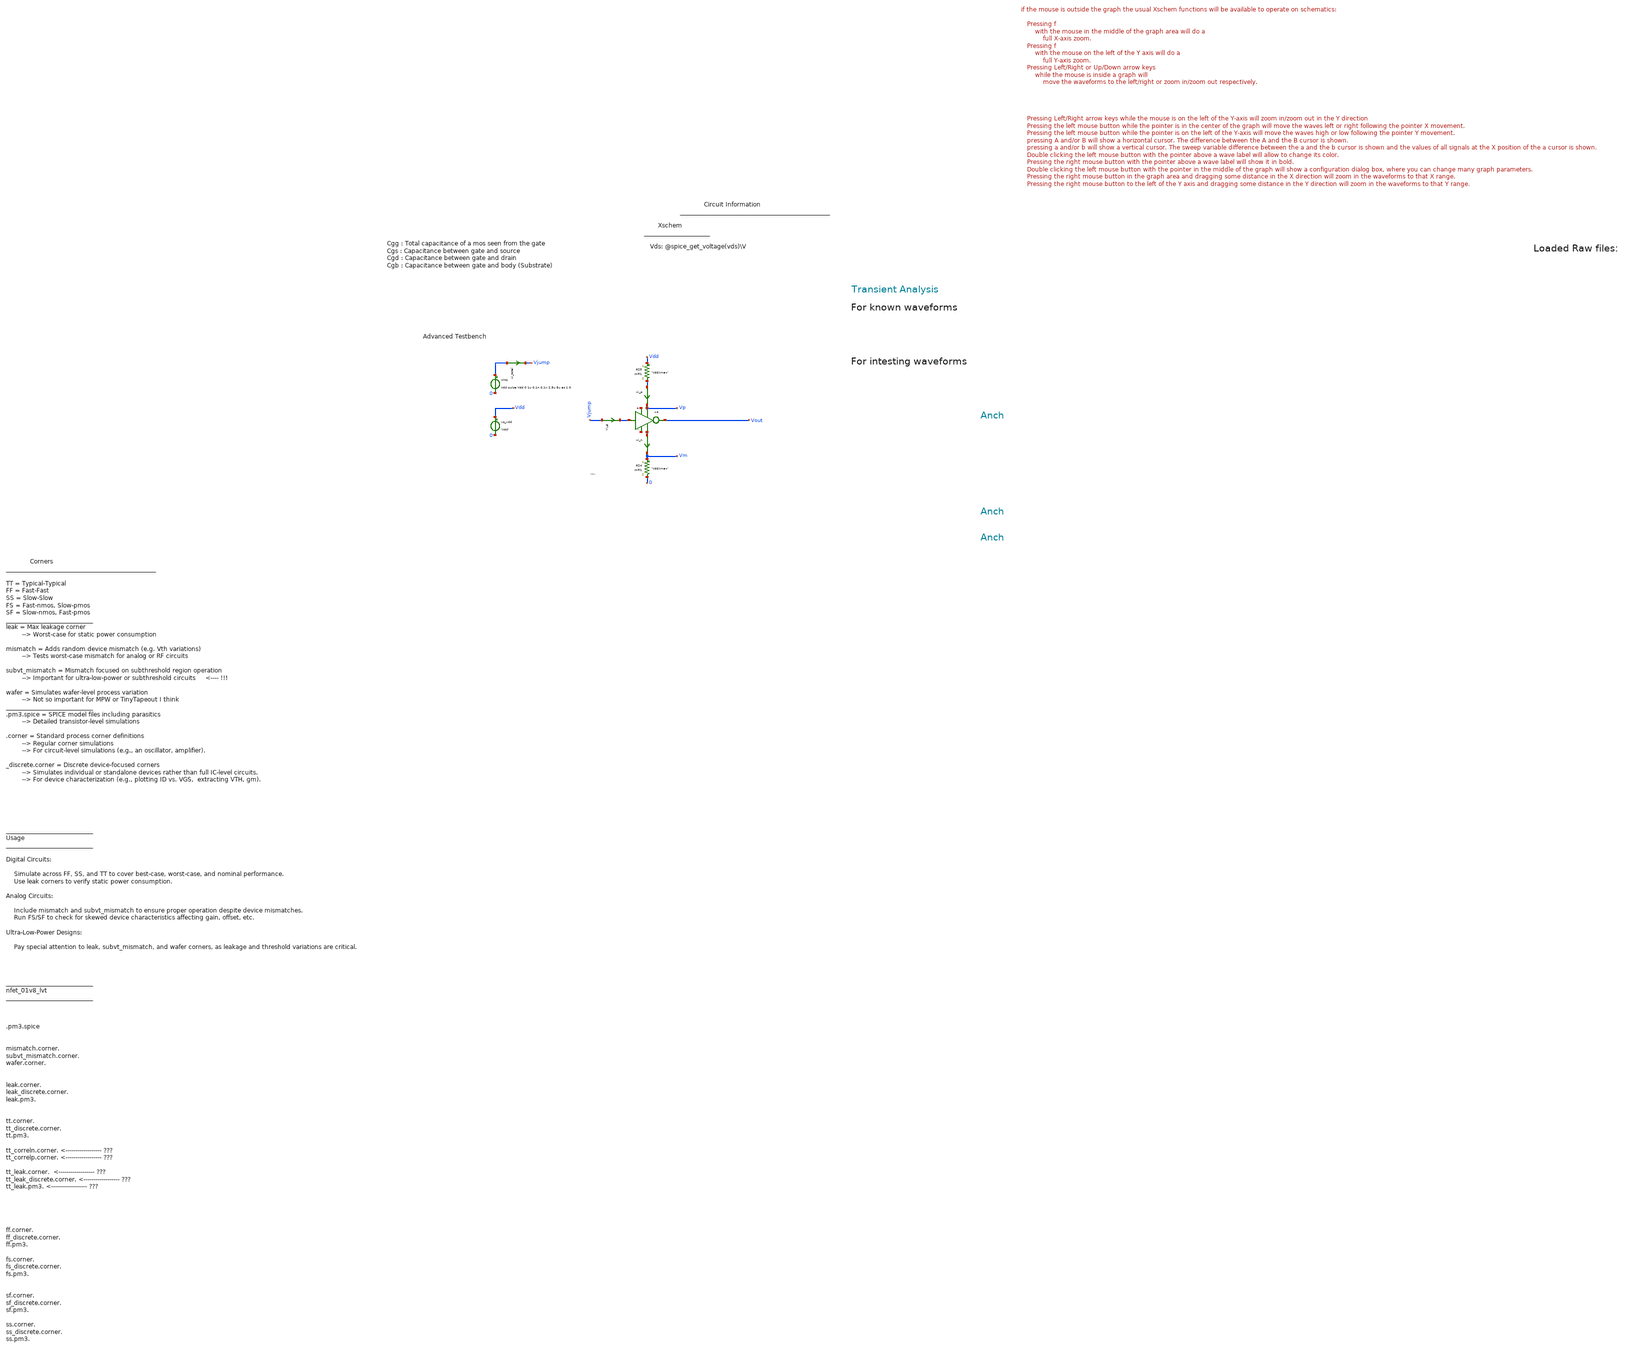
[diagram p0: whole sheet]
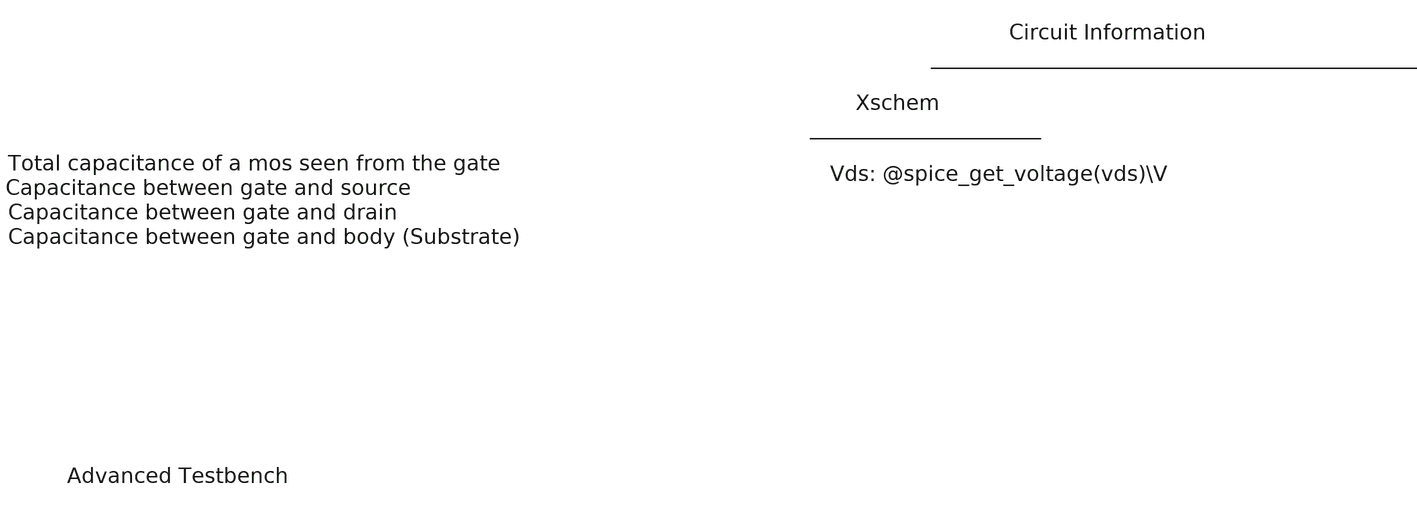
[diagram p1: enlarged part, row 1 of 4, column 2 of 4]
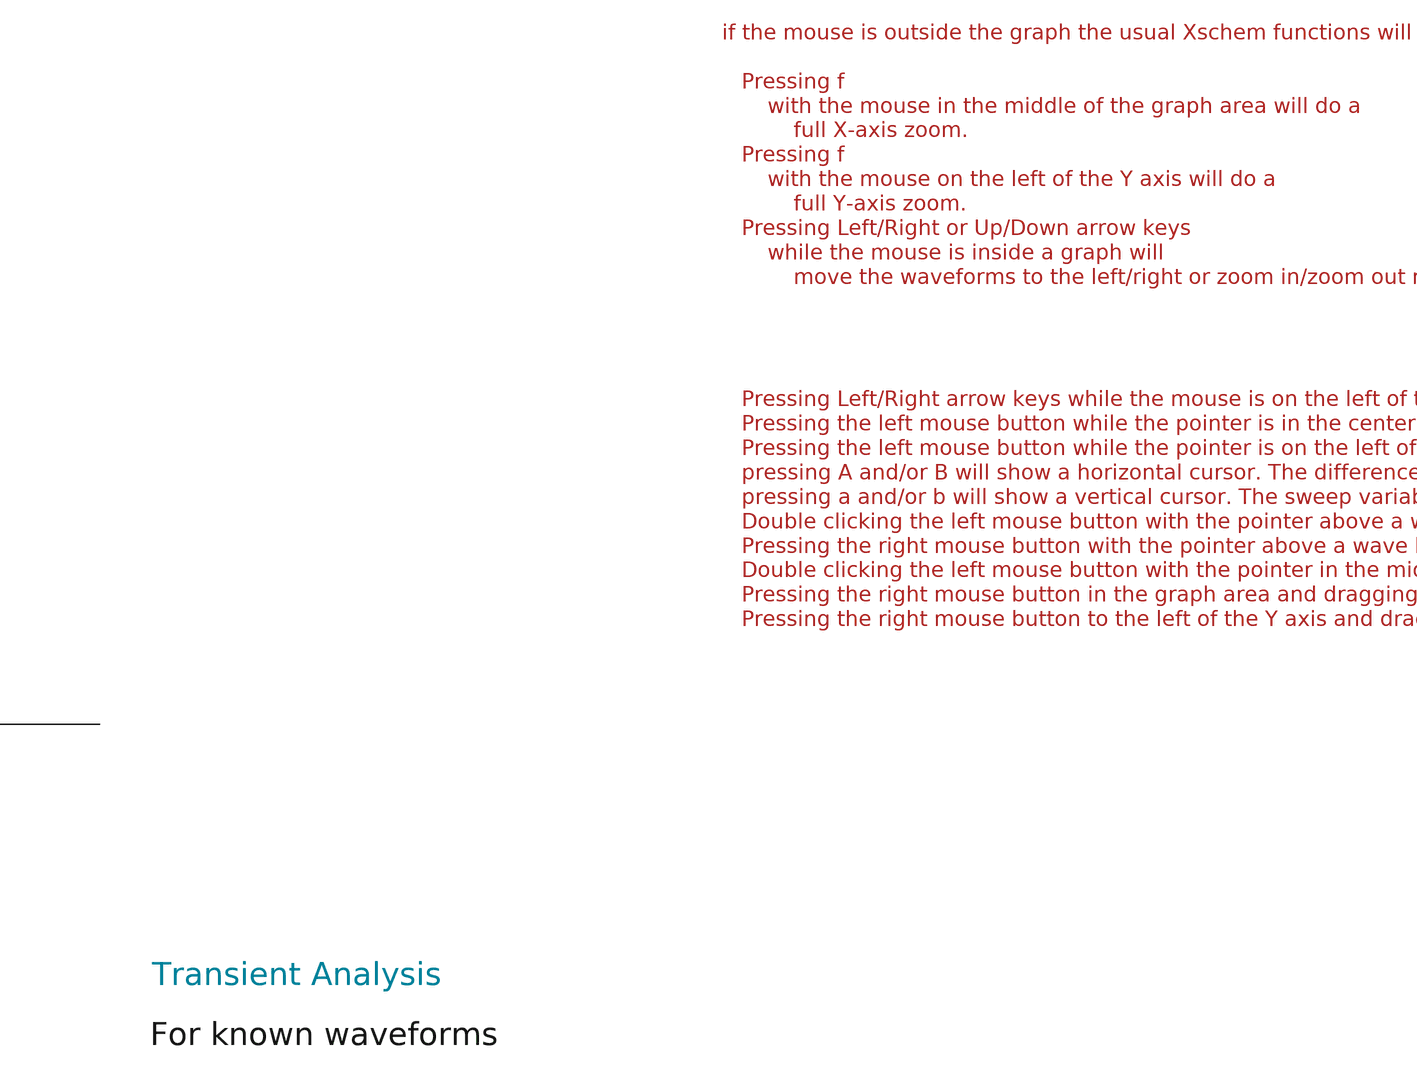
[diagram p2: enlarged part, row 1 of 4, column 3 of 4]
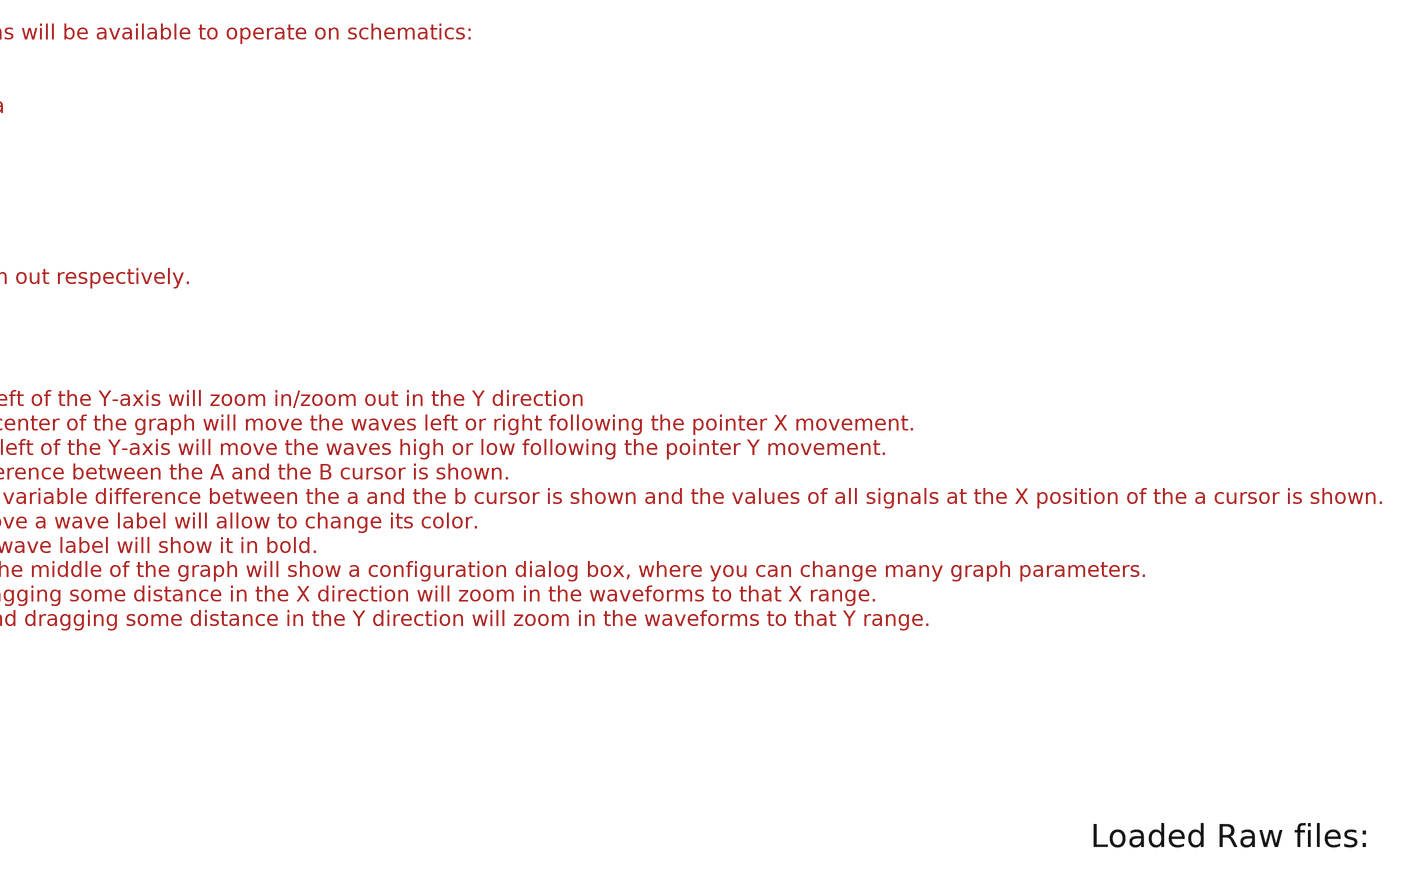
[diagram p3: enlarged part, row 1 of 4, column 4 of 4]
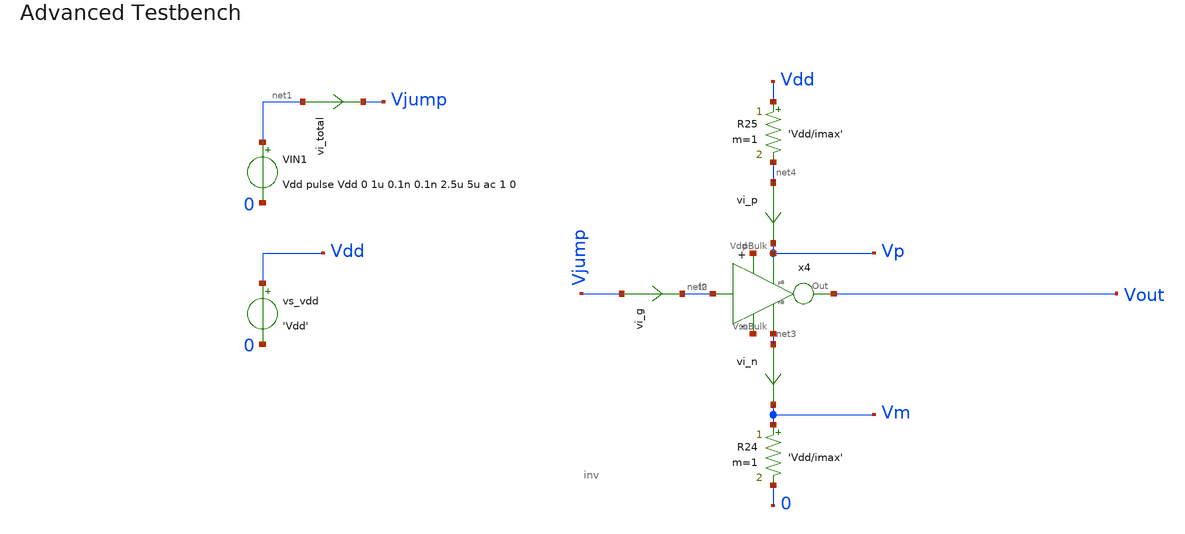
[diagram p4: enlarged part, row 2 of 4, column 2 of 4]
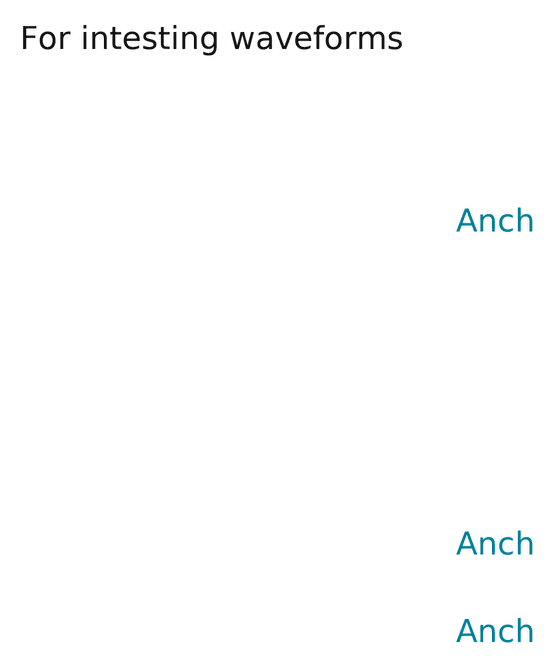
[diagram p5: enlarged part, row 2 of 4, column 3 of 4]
** sch_path: tt10-hdl/tt_um_test_commit/xschem/T0/inv/inv_Slewrate_tb.sch
* Copyright (C) 1998-2024 Stefan Frederik Schippers
* This program is free software; you can redistribute it and/or modify
* it under the terms of the GNU General Public License as published by
* the Free Software Foundation; either version 2 of the License, or
* (at your option) any later version.
* This program is distributed in the hope that it will be useful,
* but WITHOUT ANY WARRANTY; without even the implied warranty of
* MERCHANTABILITY or FITNESS FOR A PARTICULAR PURPOSE.  See the
* GNU General Public License for more details.
* You should have received a copy of the GNU General Public License
* along with this program; if not, write to the Free Software
**.subckt inv_Slewrate_tb
VIN1 net1 0 Vdd pulse Vdd 0 1u 0.1n 0.1n 2.5u 5u ac 1 0
vi_total net1 Vjump 0
.save i(vi_total)
vs_vdd Vdd 0 'Vdd'
x4 net5 net6 Vout net2 net3 Vp inv
vi_g Vjump net2 0
.save i(vi_g)
vi_p net4 Vp 0
.save i(vi_p)
vi_n net3 Vm 0
.save i(vi_n)
R24 Vm 0 'Vdd/imax' m=1
R25 Vdd net4 'Vdd/imax' m=1
**** begin user architecture code



.temp 30

*.option gmin=5n
*.option scale=1e-6
.param Vdd = 1.8
.param imax = 10e-9
.option wnflag=1
.option savecurrents

.save all
.control
  save all alli
  save @m.xm1.msky130_fd_pr__nfet_01v8[gm]
  save @m.xm1.msky130_fd_pr__nfet_01v8[id]
  save @m.xm1.msky130_fd_pr__nfet_01v8[vgs]

  save @m.xm1.msky130_fd_pr__nfet_01v8[cgg]
  save @m.xm1.msky130_fd_pr__nfet_01v8[cgs]
  save @m.xm1.msky130_fd_pr__nfet_01v8[cgdo]
  save @m.xm1.msky130_fd_pr__nfet_01v8[cgb]

  save @m.xm1.msky130_fd_pr__nfet_01v8[vds]
  save @m.xm1.msky130_fd_pr__nfet_01v8[vdsat]
  save @m.xm1.msky130_fd_pr__nfet_01v8[vth]


  save @m.xm1.msky130_fd_pr__nfet_01v8[leff]
  save @m.xm1.msky130_fd_pr__nfet_01v8[weff]
  save @m.xm1.msky130_fd_pr__nfet_01v8[gds]
  save @m.xm1.msky130_fd_pr__nfet_01v8[l]
  save @m.xm1.msky130_fd_pr__nfet_01v8[w]
  save @m.xm1.msky130_fd_pr__nfet_01v8[gm]
  save @m.xm1.msky130_fd_pr__nfet_01v8[gm]
  save @m.xm1.msky130_fd_pr__nfet_01v8[gm]
  save @m.xm1.msky130_fd_pr__nfet_01v8[gm]
  save @m.xm1.msky130_fd_pr__nfet_01v8[gm]






  tran 1n 7u
  remzerovec
  write nmos_tb_tran.raw

  op
  set appendwrite
  remzerovec
  write nmos_tb_tran.raw






  *quit 0




.endc





** opencircuitdesign pdks install
.lib $::SKYWATER_MODELS/sky130.lib.spice tt
.include $::SKYWATER_STDCELLS/sky130_fd_sc_hd.spice


**** end user architecture code
**.ends

* expanding   symbol:  T0/inv/inv.sym # of pins=6
** sym_path: tt10-hdl/tt_um_test_commit/xschem/T0/inv/inv.sym
** sch_path: tt10-hdl/tt_um_test_commit/xschem/T0/inv/inv.sch
.subckt inv Vdd Vss Out In nBulk pBulk
*.ipin Vdd
*.ipin Vss
*.opin Out
*.ipin In
*.ipin nBulk
*.ipin pBulk
XM1 Out In Vss nBulk sky130_fd_pr__nfet_01v8 L=0.15 W=1 nf=1 ad='int((1 + 1)/2) * 1 / 1 * 0.29' as='int((1 + 2)/2) * 1 / 1 * 0.29'
+ pd='2*int((1 + 1)/2) * (1 / 1 + 0.29)' ps='2*int((1 + 2)/2) * (1 / 1 + 0.29)' nrd='0.29 / 1 ' nrs='0.29 / 1 '
+ sa=0 sb=0 sd=0 mult=1 m=1
XM2 Out In Vdd pBulk sky130_fd_pr__pfet_01v8 L=0.15 W=1 nf=1 ad='int((nf+1)/2) * W/nf * 0.29' as='int((nf+2)/2) * W/nf * 0.29'
+ pd='2*int((nf+1)/2) * (W/nf + 0.29)' ps='2*int((nf+2)/2) * (W/nf + 0.29)' nrd='0.29 / W' nrs='0.29 / W'
+ sa=0 sb=0 sd=0 mult=1 m=1
.ends

.end
